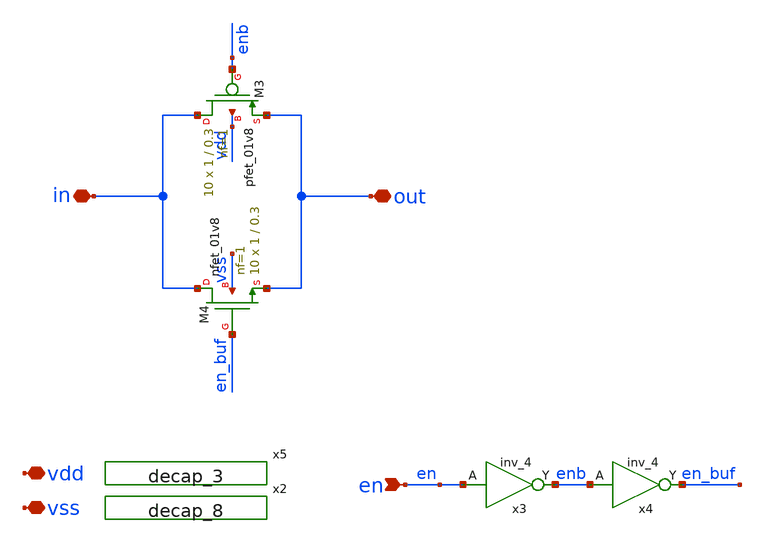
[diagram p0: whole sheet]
** sch_path: xschem/sar/sw/sw_top.sch
**.subckt sw_top out en vss vdd in
*.iopin out
*.ipin en
*.iopin vss
*.iopin vdd
*.iopin in
XM3 in enb out vdd sky130_fd_pr__pfet_01v8 L=0.3 W=1 nf=1 ad='int((nf+1)/2) * W/nf * 0.29' as='int((nf+2)/2) * W/nf * 0.29'
+ pd='2*int((nf+1)/2) * (W/nf + 0.29)' ps='2*int((nf+2)/2) * (W/nf + 0.29)' nrd='0.29 / W' nrs='0.29 / W'
+ sa=0 sb=0 sd=0 mult=10 m=10
XM4 in en_buf out vss sky130_fd_pr__nfet_01v8 L=0.3 W=1 nf=1 ad='int((nf+1)/2) * W/nf * 0.29' as='int((nf+2)/2) * W/nf * 0.29'
+ pd='2*int((nf+1)/2) * (W/nf + 0.29)' ps='2*int((nf+2)/2) * (W/nf + 0.29)' nrd='0.29 / W' nrs='0.29 / W'
+ sa=0 sb=0 sd=0 mult=10 m=10
x2 vss vss vdd vdd sky130_fd_sc_hd__decap_8
x3 en vss vss vdd vdd enb sky130_fd_sc_hd__inv_4
x4 enb vss vss vdd vdd en_buf sky130_fd_sc_hd__inv_4
x5 vss vss vdd vdd sky130_fd_sc_hd__decap_3
**.ends
.end
